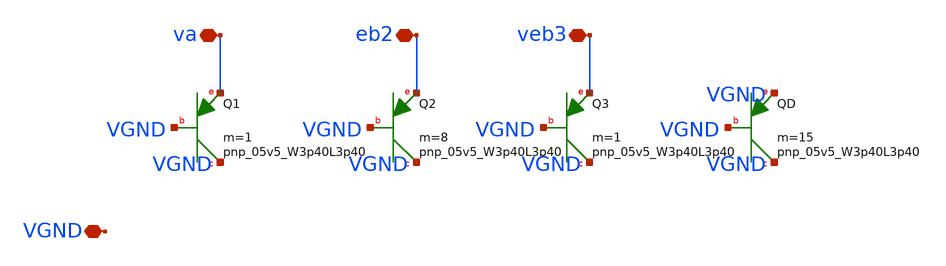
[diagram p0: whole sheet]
** sch_path: xschem/bg_pnp.sch
**.subckt bg_pnp va eb2 veb3 VGND
*.iopin va
*.iopin eb2
*.iopin veb3
*.iopin VGND
XQ1 VGND VGND va sky130_fd_pr__pnp_05v5_W3p40L3p40 m=1
XQ2 VGND VGND eb2 sky130_fd_pr__pnp_05v5_W3p40L3p40 m=8
XQ3 VGND VGND veb3 sky130_fd_pr__pnp_05v5_W3p40L3p40 m=1
XQD VGND VGND VGND sky130_fd_pr__pnp_05v5_W3p40L3p40 m=15
**.ends
.end
